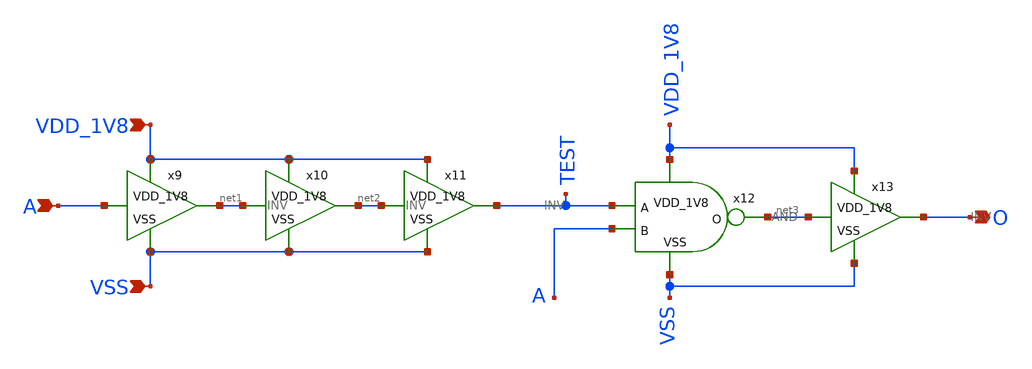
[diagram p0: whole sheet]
** sch_path: design/CNR_GR05_SKY130NM/POSEDGE.sch
**.subckt POSEDGE VDD_1V8 VSS O A
*.ipin VDD_1V8
*.ipin VSS
*.opin O
*.ipin A
x9 VDD_1V8 A net1 VSS INV
x10 VDD_1V8 net1 net2 VSS INV
x11 VDD_1V8 net2 TEST VSS INV
x12 VDD_1V8 TEST A net3 VSS AND
x13 VDD_1V8 net3 O VSS INV
**.ends
.end
